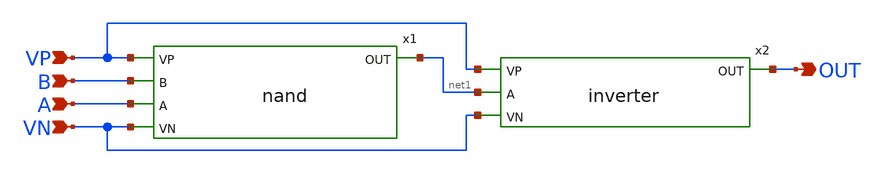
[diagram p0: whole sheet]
** sch_path: basic_cell/and/xschem/and.sch
**.subckt and VP B A VN OUT
*.ipin VP
*.ipin B
*.ipin A
*.ipin VN
*.opin OUT
x1 VP net1 B A VN nand
x2 VP net1 OUT VN inverter
**.ends

* expanding   symbol:  /foss/designs/APIC_Mux_DFF/basic_cell/single_cell/nand/nand.sym # of pins=5
** sym_path: basic_cell/single_cell/nand/nand.sym
** sch_path: basic_cell/single_cell/nand/nand.sch
.subckt nand VP OUT B A VN
*.opin OUT
*.ipin A
*.ipin B
*.ipin VN
*.ipin VP
XM4 OUT A net1 VN sky130_fd_pr__nfet_01v8 L=0.15 W=1 nf=1 ad='int((nf+1)/2) * W/nf * 0.29' as='int((nf+2)/2) * W/nf * 0.29'
+ pd='2*int((nf+1)/2) * (W/nf + 0.29)' ps='2*int((nf+2)/2) * (W/nf + 0.29)' nrd='0.29 / W' nrs='0.29 / W'
+ sa=0 sb=0 sd=0 mult=1 m=1
XM3 net1 B VN VN sky130_fd_pr__nfet_01v8 L=0.15 W=1 nf=1 ad='int((nf+1)/2) * W/nf * 0.29' as='int((nf+2)/2) * W/nf * 0.29'
+ pd='2*int((nf+1)/2) * (W/nf + 0.29)' ps='2*int((nf+2)/2) * (W/nf + 0.29)' nrd='0.29 / W' nrs='0.29 / W'
+ sa=0 sb=0 sd=0 mult=1 m=1
XM1 OUT A VP VP sky130_fd_pr__pfet_01v8 L=0.15 W=3 nf=1 ad='int((nf+1)/2) * W/nf * 0.29' as='int((nf+2)/2) * W/nf * 0.29'
+ pd='2*int((nf+1)/2) * (W/nf + 0.29)' ps='2*int((nf+2)/2) * (W/nf + 0.29)' nrd='0.29 / W' nrs='0.29 / W'
+ sa=0 sb=0 sd=0 mult=1 m=1
XM2 OUT B VP VP sky130_fd_pr__pfet_01v8 L=0.15 W=3 nf=1 ad='int((nf+1)/2) * W/nf * 0.29' as='int((nf+2)/2) * W/nf * 0.29'
+ pd='2*int((nf+1)/2) * (W/nf + 0.29)' ps='2*int((nf+2)/2) * (W/nf + 0.29)' nrd='0.29 / W' nrs='0.29 / W'
+ sa=0 sb=0 sd=0 mult=1 m=1
.ends


* expanding   symbol:  /foss/designs/APIC_Mux_DFF/basic_cell/single_cell/inverter/inverter.sym # of
*+ pins=4
** sym_path: basic_cell/single_cell/inverter/inverter.sym
** sch_path: basic_cell/single_cell/inverter/inverter.sch
.subckt inverter VP A OUT VN
*.ipin A
*.ipin VP
*.ipin VN
*.opin OUT
XM1 OUT A VP VP sky130_fd_pr__pfet_01v8 L=0.15 W=3 nf=1 ad='int((nf+1)/2) * W/nf * 0.29' as='int((nf+2)/2) * W/nf * 0.29'
+ pd='2*int((nf+1)/2) * (W/nf + 0.29)' ps='2*int((nf+2)/2) * (W/nf + 0.29)' nrd='0.29 / W' nrs='0.29 / W'
+ sa=0 sb=0 sd=0 mult=1 m=1
XM2 OUT A VN VN sky130_fd_pr__nfet_01v8 L=0.15 W=1 nf=1 ad='int((nf+1)/2) * W/nf * 0.29' as='int((nf+2)/2) * W/nf * 0.29'
+ pd='2*int((nf+1)/2) * (W/nf + 0.29)' ps='2*int((nf+2)/2) * (W/nf + 0.29)' nrd='0.29 / W' nrs='0.29 / W'
+ sa=0 sb=0 sd=0 mult=1 m=1
.ends

.end
